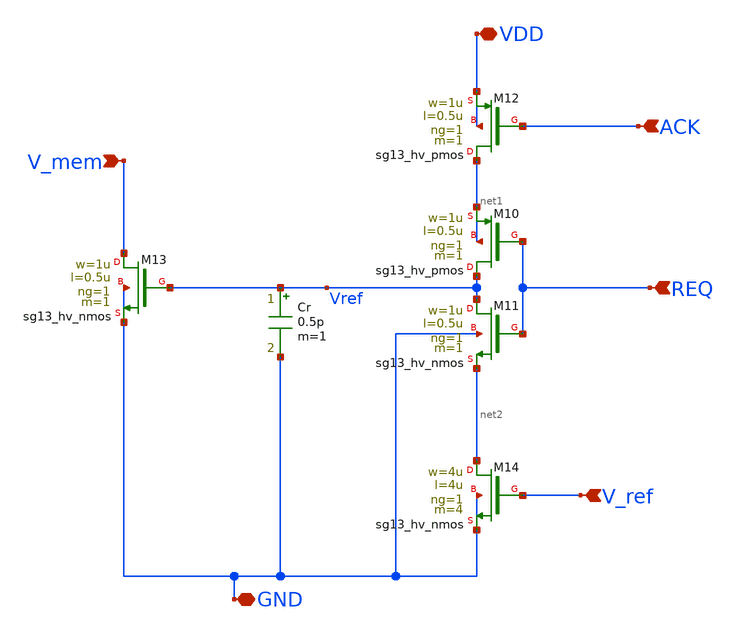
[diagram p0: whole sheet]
** sch_path: xschem/REF_system.sch
**.subckt REF_system VDD GND V_ref REQ ACK V_mem
*.iopin VDD
*.iopin GND
*.ipin V_ref
*.ipin REQ
*.ipin ACK
*.ipin V_mem
Cr Vref GND 0.5p m=1
XM10 Vref REQ net1 net1 sg13_hv_pmos w=1u l=0.5u ng=1 m=1 mm_ok=1
XM11 Vref REQ net2 GND sg13_hv_nmos w=1u l=0.5u ng=1 m=1 mm_ok=1
XM12 net1 ACK VDD VDD sg13_hv_pmos w=1u l=0.5u ng=1 m=1 mm_ok=1
XM13 V_mem Vref GND GND sg13_hv_nmos w=1u l=0.5u ng=1 m=1 mm_ok=1
XM14 net2 V_ref GND GND sg13_hv_nmos w=4u l=4u ng=1 m=4 mm_ok=1
**.ends
.end
